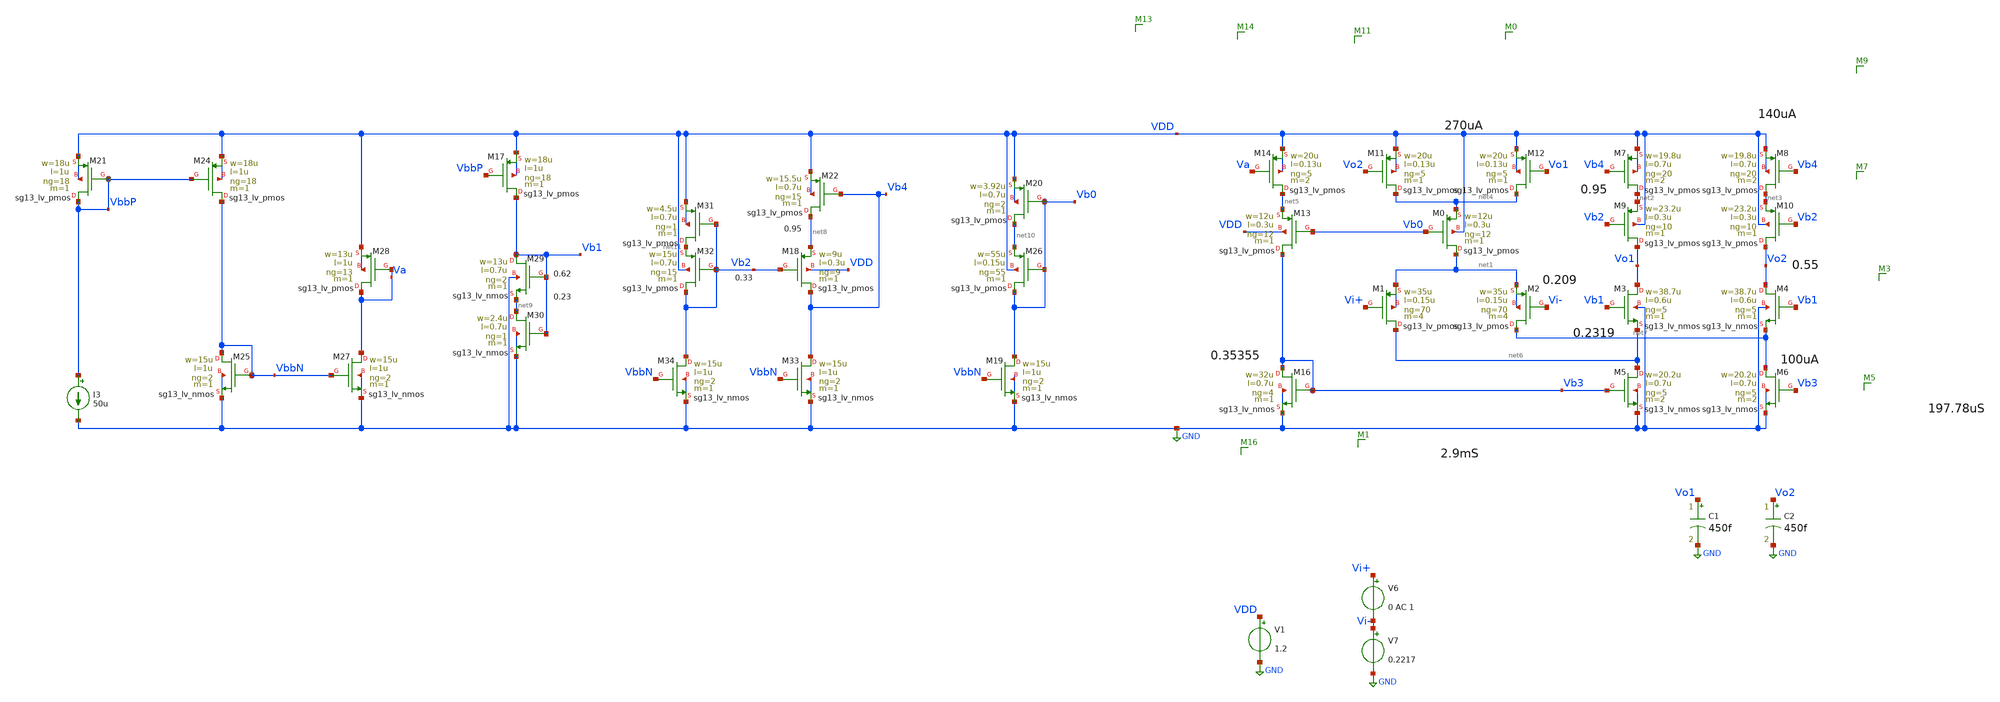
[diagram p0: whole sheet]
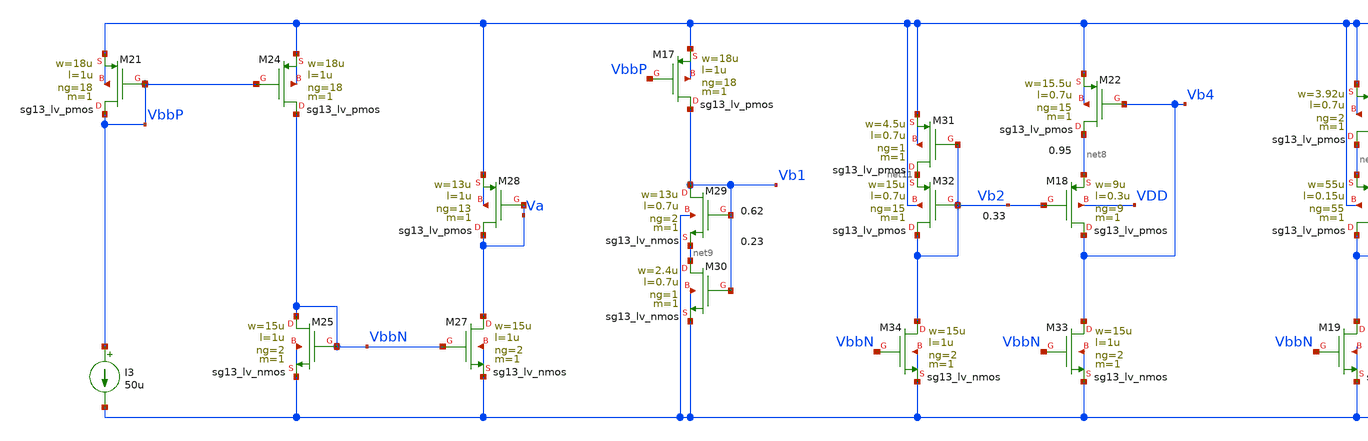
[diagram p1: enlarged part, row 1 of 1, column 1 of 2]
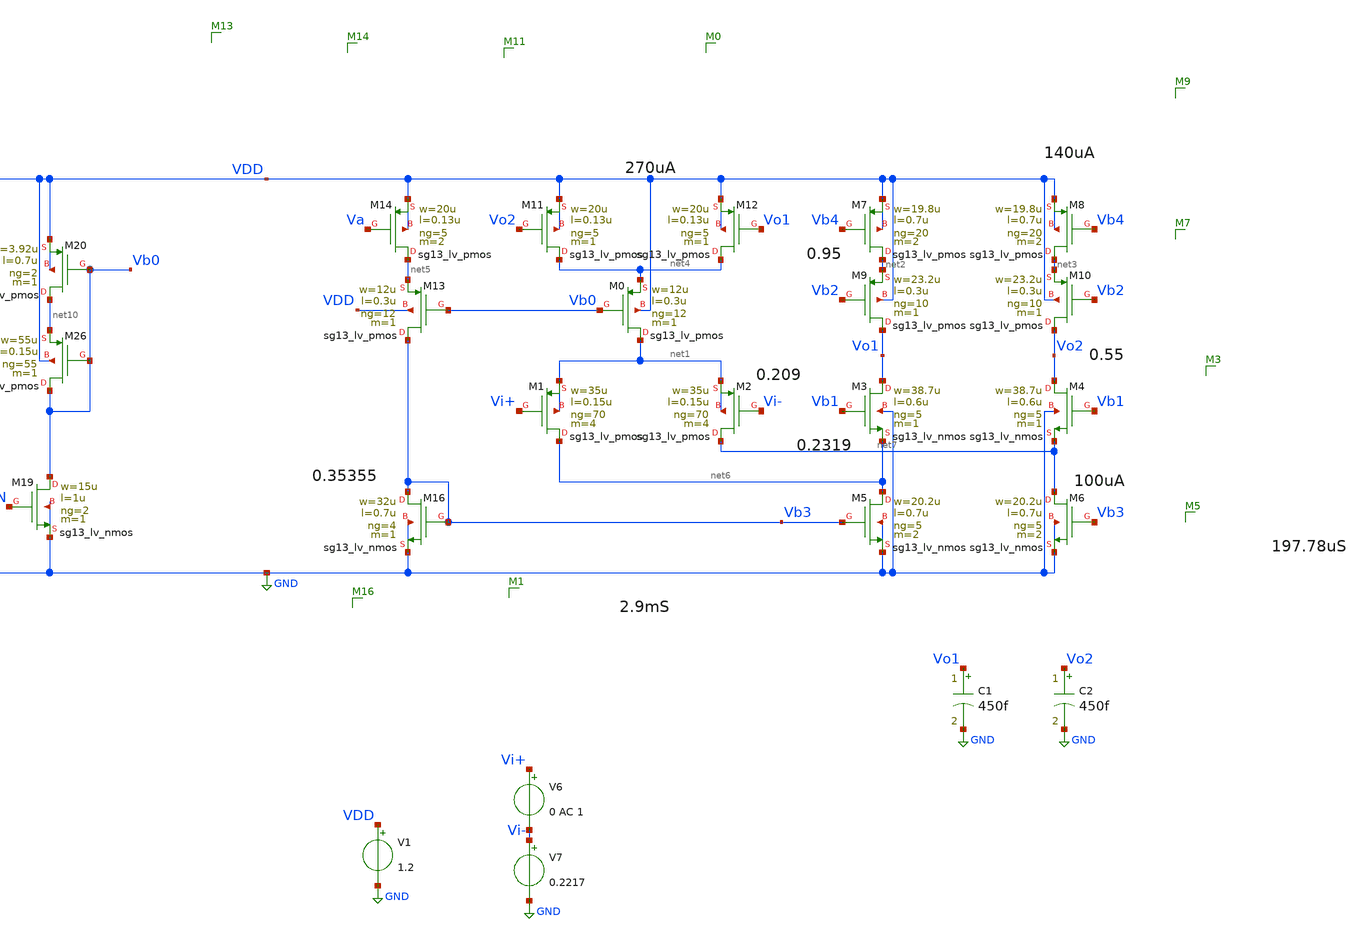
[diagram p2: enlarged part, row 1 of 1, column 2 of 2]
** sch_path: sch/testing/gmBoosting.sch
**.subckt gmBoosting
XM7 net2 Vb4 VDD VDD sg13_lv_pmos w=19.8u l=0.7u ng=20 m=2 mm_ok=1
XM1 net6 Vi+ net1 net1 sg13_lv_pmos w=35u l=0.15u ng=70 m=4 mm_ok=1
XM2 net7 Vi- net1 net1 sg13_lv_pmos w=35u l=0.15u ng=70 m=4 mm_ok=1
XM0 net1 Vb0 net4 VDD sg13_lv_pmos w=12u l=0.3u ng=12 m=1 mm_ok=1
V1 VDD GND 1.2
V7 Vi- GND 0.2217
V6 Vi+ Vi- 0 AC 1
C1 Vo1 GND 450f m=1
C2 Vo2 GND 450f m=1
XM9 Vo1 Vb2 net2 VDD sg13_lv_pmos w=23.2u l=0.3u ng=10 m=1 mm_ok=1
XM10 Vo2 Vb2 net3 VDD sg13_lv_pmos w=23.2u l=0.3u ng=10 m=1 mm_ok=1
XM8 net3 Vb4 VDD VDD sg13_lv_pmos w=19.8u l=0.7u ng=20 m=2 mm_ok=1
XM11 net4 Vo2 VDD VDD sg13_lv_pmos w=20u l=0.13u ng=5 m=1 mm_ok=1
XM12 net4 Vo1 VDD VDD sg13_lv_pmos w=20u l=0.13u ng=5 m=1 mm_ok=1
XM14 net5 Va VDD VDD sg13_lv_pmos w=20u l=0.13u ng=5 m=2 mm_ok=1
XM16 Vb3 Vb3 GND GND sg13_lv_nmos w=32u l=0.7u ng=4 m=1 mm_ok=1
XM13 Vb3 Vb0 net5 VDD sg13_lv_pmos w=12u l=0.3u ng=12 m=1 mm_ok=1
I3 VbbP GND 50u
XM21 VbbP VbbP VDD VDD sg13_lv_pmos w=18u l=1u ng=18 m=1 mm_ok=1
XM24 VbbN VbbP VDD VDD sg13_lv_pmos w=18u l=1u ng=18 m=1 mm_ok=1
XM25 VbbN VbbN GND GND sg13_lv_nmos w=15u l=1u ng=2 m=1 mm_ok=1
XM27 Va VbbN GND GND sg13_lv_nmos w=15u l=1u ng=2 m=1 mm_ok=1
XM28 Va Va VDD VDD sg13_lv_pmos w=13u l=1u ng=13 m=1 mm_ok=1
XM29 Vb1 Vb1 net9 GND sg13_lv_nmos w=13u l=0.7u ng=2 m=1 mm_ok=1
XM30 net9 Vb1 GND GND sg13_lv_nmos w=2.4u l=0.7u ng=1 m=1 mm_ok=1
XM17 Vb1 VbbP VDD VDD sg13_lv_pmos w=18u l=1u ng=18 m=1 mm_ok=1
XM18 Vb4 Vb2 net8 VDD sg13_lv_pmos w=9u l=0.3u ng=9 m=1 mm_ok=1
XM22 net8 Vb4 VDD VDD sg13_lv_pmos w=15.5u l=0.7u ng=15 m=1 mm_ok=1
XM33 Vb4 VbbN GND GND sg13_lv_nmos w=15u l=1u ng=2 m=1 mm_ok=1
XM31 net11 Vb2 VDD VDD sg13_lv_pmos w=4.5u l=0.7u ng=1 m=1 mm_ok=1
XM32 Vb2 Vb2 net11 VDD sg13_lv_pmos w=15u l=0.7u ng=15 m=1 mm_ok=1
XM34 Vb2 VbbN GND GND sg13_lv_nmos w=15u l=1u ng=2 m=1 mm_ok=1
XM3 Vo1 Vb1 net6 GND sg13_lv_nmos w=38.7u l=0.6u ng=5 m=1 mm_ok=1
XM4 Vo2 Vb1 net7 GND sg13_lv_nmos w=38.7u l=0.6u ng=5 m=1 mm_ok=1
XM5 net6 Vb3 GND GND sg13_lv_nmos w=20.2u l=0.7u ng=5 m=2 mm_ok=1
XM6 net7 Vb3 GND GND sg13_lv_nmos w=20.2u l=0.7u ng=5 m=2 mm_ok=1
XM19 Vb0 VbbN GND GND sg13_lv_nmos w=15u l=1u ng=2 m=1 mm_ok=1
XM20 net10 Vb0 VDD VDD sg13_lv_pmos w=3.92u l=0.7u ng=2 m=1 mm_ok=1
XM26 Vb0 Vb0 net10 VDD sg13_lv_pmos w=55u l=0.15u ng=55 m=1 mm_ok=1
**** begin user architecture code



.include gmBoosting.save
.lib cornerMOSlv.lib mos_tt
.lib cornerRES.lib res_typ
.temp 65
.control
save all
op
write gmBoosting.raw


ac dec 1k 1 10G
let Av = db((v(Vo1)-v(Vo2)))
meas ac UGBW WHEN Av=0
let phase_vec = 180/pi*cph(v(Vo1)-v(Vo2))

meas ac phase FIND phase_vec WHEN frequency=UGBW
let PM = phase
print PM

plot Av
plot phase_vec



.endc



**** end user architecture code
**.ends
.GLOBAL GND
.end
